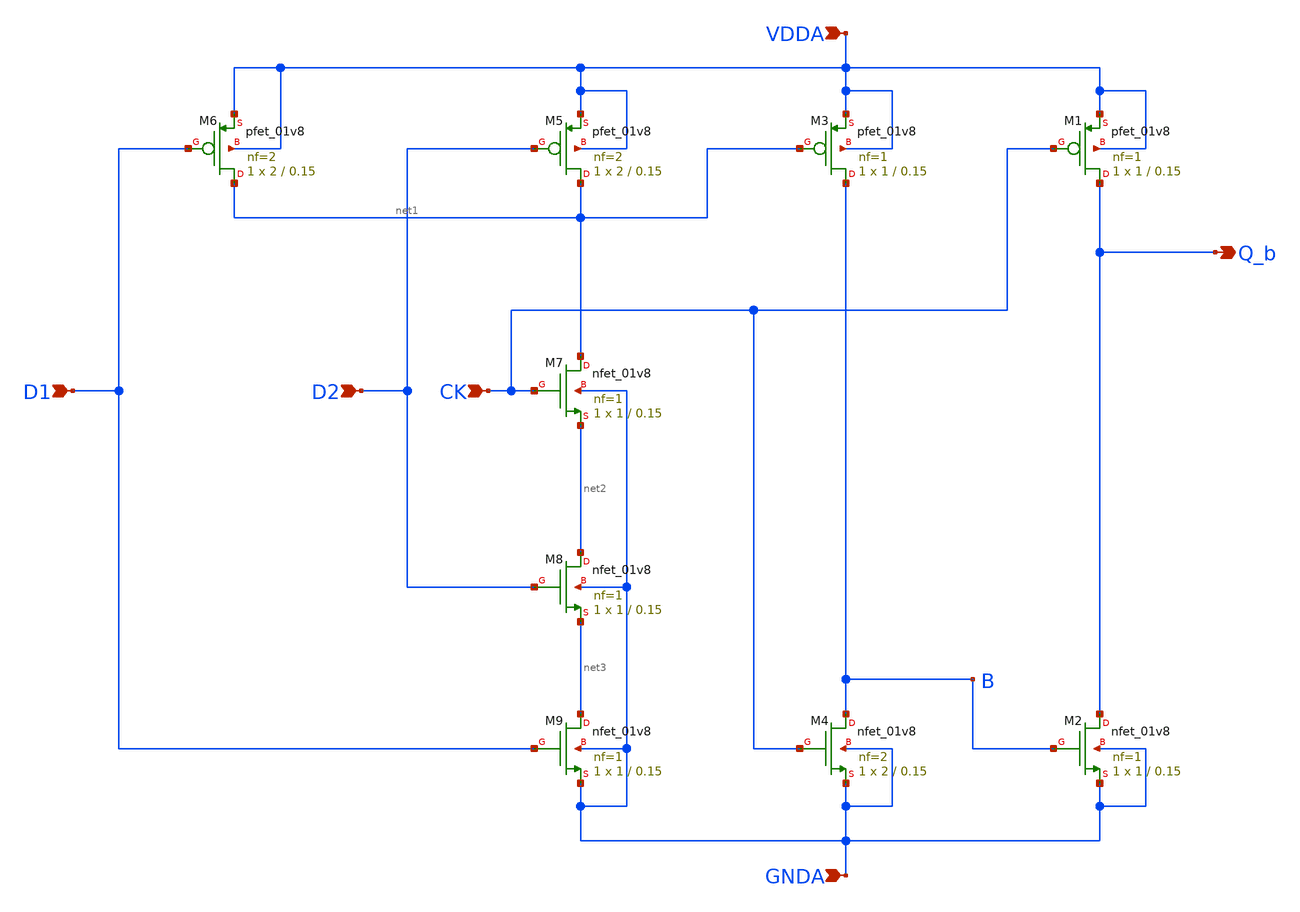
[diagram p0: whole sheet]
** sch_path: projects/pll/divider/xschem_ngspice/TSPC_FF_ratioed_nand.sch
**.subckt TSPC_FF_ratioed_nand CK D1 Q_b VDDA GNDA D2
*.ipin CK
*.ipin D1
*.opin Q_b
*.ipin VDDA
*.ipin GNDA
*.ipin D2
XM1 Q_b CK VDDA VDDA sky130_fd_pr__pfet_01v8 L=0.15 W=1 nf=1 ad='int((nf+1)/2) * W/nf * 0.29' as='int((nf+2)/2) * W/nf * 0.29'
+ pd='2*int((nf+1)/2) * (W/nf + 0.29)' ps='2*int((nf+2)/2) * (W/nf + 0.29)' nrd='0.29 / W' nrs='0.29 / W'
+ sa=0 sb=0 sd=0 mult=1 m=1
XM2 Q_b B GNDA GNDA sky130_fd_pr__nfet_01v8 L=0.15 W=1 nf=1 ad='int((nf+1)/2) * W/nf * 0.29' as='int((nf+2)/2) * W/nf * 0.29'
+ pd='2*int((nf+1)/2) * (W/nf + 0.29)' ps='2*int((nf+2)/2) * (W/nf + 0.29)' nrd='0.29 / W' nrs='0.29 / W'
+ sa=0 sb=0 sd=0 mult=1 m=1
XM3 B net1 VDDA VDDA sky130_fd_pr__pfet_01v8 L=0.15 W=1 nf=1 ad='int((nf+1)/2) * W/nf * 0.29' as='int((nf+2)/2) * W/nf * 0.29'
+ pd='2*int((nf+1)/2) * (W/nf + 0.29)' ps='2*int((nf+2)/2) * (W/nf + 0.29)' nrd='0.29 / W' nrs='0.29 / W'
+ sa=0 sb=0 sd=0 mult=1 m=1
XM4 B CK GNDA GNDA sky130_fd_pr__nfet_01v8 L=0.15 W=2 nf=2 ad='int((nf+1)/2) * W/nf * 0.29' as='int((nf+2)/2) * W/nf * 0.29'
+ pd='2*int((nf+1)/2) * (W/nf + 0.29)' ps='2*int((nf+2)/2) * (W/nf + 0.29)' nrd='0.29 / W' nrs='0.29 / W'
+ sa=0 sb=0 sd=0 mult=1 m=1
XM5 net1 D2 VDDA VDDA sky130_fd_pr__pfet_01v8 L=0.15 W=2 nf=2 ad='int((nf+1)/2) * W/nf * 0.29' as='int((nf+2)/2) * W/nf * 0.29'
+ pd='2*int((nf+1)/2) * (W/nf + 0.29)' ps='2*int((nf+2)/2) * (W/nf + 0.29)' nrd='0.29 / W' nrs='0.29 / W'
+ sa=0 sb=0 sd=0 mult=1 m=1
XM9 net3 D1 GNDA GNDA sky130_fd_pr__nfet_01v8 L=0.15 W=1 nf=1 ad='int((nf+1)/2) * W/nf * 0.29' as='int((nf+2)/2) * W/nf * 0.29'
+ pd='2*int((nf+1)/2) * (W/nf + 0.29)' ps='2*int((nf+2)/2) * (W/nf + 0.29)' nrd='0.29 / W' nrs='0.29 / W'
+ sa=0 sb=0 sd=0 mult=1 m=1
XM7 net1 CK net2 GNDA sky130_fd_pr__nfet_01v8 L=0.15 W=1 nf=1 ad='int((nf+1)/2) * W/nf * 0.29' as='int((nf+2)/2) * W/nf * 0.29'
+ pd='2*int((nf+1)/2) * (W/nf + 0.29)' ps='2*int((nf+2)/2) * (W/nf + 0.29)' nrd='0.29 / W' nrs='0.29 / W'
+ sa=0 sb=0 sd=0 mult=1 m=1
XM6 net1 D1 VDDA VDDA sky130_fd_pr__pfet_01v8 L=0.15 W=2 nf=2 ad='int((nf+1)/2) * W/nf * 0.29' as='int((nf+2)/2) * W/nf * 0.29'
+ pd='2*int((nf+1)/2) * (W/nf + 0.29)' ps='2*int((nf+2)/2) * (W/nf + 0.29)' nrd='0.29 / W' nrs='0.29 / W'
+ sa=0 sb=0 sd=0 mult=1 m=1
XM8 net2 D2 net3 GNDA sky130_fd_pr__nfet_01v8 L=0.15 W=1 nf=1 ad='int((nf+1)/2) * W/nf * 0.29' as='int((nf+2)/2) * W/nf * 0.29'
+ pd='2*int((nf+1)/2) * (W/nf + 0.29)' ps='2*int((nf+2)/2) * (W/nf + 0.29)' nrd='0.29 / W' nrs='0.29 / W'
+ sa=0 sb=0 sd=0 mult=1 m=1
**.ends
.end
